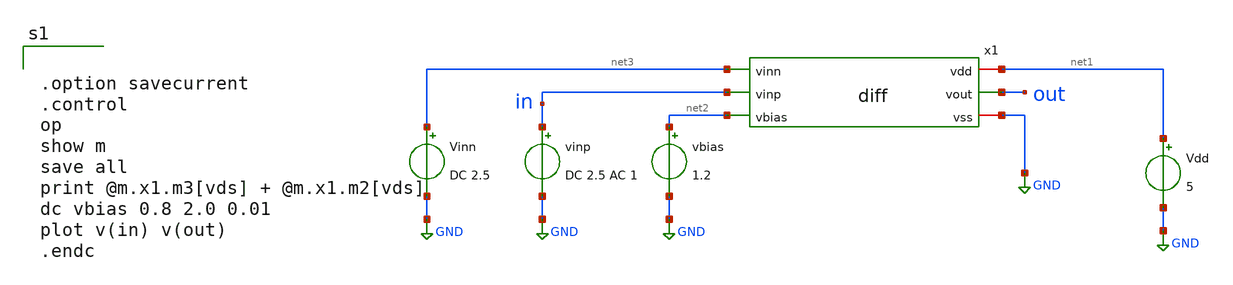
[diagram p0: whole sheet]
** sch_path: diff_dc.sch
**.subckt diff_dc
x1 net1 out net3 in net2 GND diff
Vinn net3 GND DC 2.5
vinp in GND DC 2.5 AC 1
vbias net2 GND 1.2
Vdd net1 GND 5
**** begin user architecture code
 .include $::LIB/mos.lib
.include $::LIB/passive.lib
.include $::LIB/diode.lib


.option savecurrent
.control
op
show m
save all
print @m.x1.m3[vds] + @m.x1.m2[vds]
dc vbias 0.8 2.0 0.01
plot v(in) v(out)
.endc


**** end user architecture code
**.ends

* expanding   symbol:  diff.sym # of pins=6
** sym_path: diff.sym
** sch_path: diff.sch
.subckt diff vdd vout vinn vinp vbias vss
*.iopin vss
*.iopin vdd
*.ipin vinn
*.ipin vinp
*.opin vout
*.ipin vbias
M1 net1 vinn net2 vss nmos L=1u W=10u m=1
M2 vout vinp net2 vss nmos L=1u W=10u m=1
M3 net2 vbias vss vss nmos L=1u W=20u m=1
M4 net1 net1 vdd vdd pmos L=1u W=30u m=1
M5 vout net1 vdd vdd pmos L=1u W=30u m=1
.ends

.GLOBAL GND
.end
